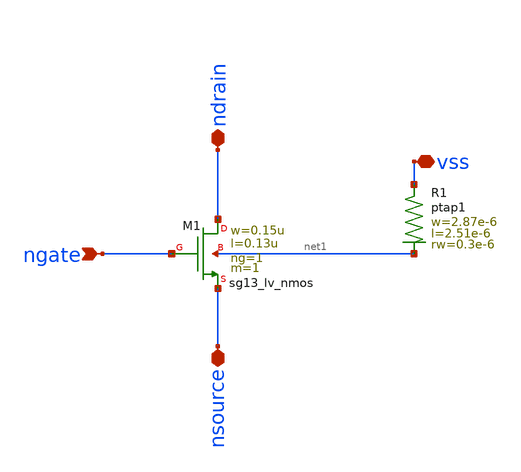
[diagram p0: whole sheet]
** sch_path: ihp-sg13g2/libs.tech/klayout/sg13g2_tests/lvs_testcases/nmos_test.sch
**.subckt nmos_test vss ngate ndrain nsource
*.iopin vss
*.ipin ngate
*.iopin ndrain
*.iopin nsource
XM1 ndrain ngate nsource net1 sg13_lv_nmos w=0.15u l=0.13u ng=1 m=1 mm_ok=1
XR1 vss net1 ptap1 R=23.84 w=2.87e-6 l=2.51e-6
**.ends
.end
